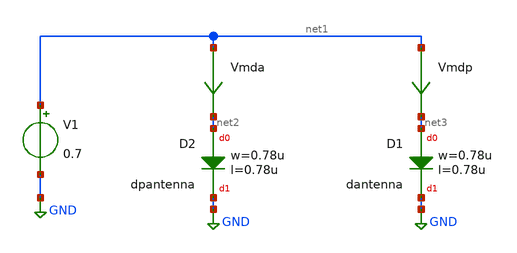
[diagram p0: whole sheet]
** sch_path: ihp-sg13g2/xschem_libs/sg13g2_tests_ase/dc_diode_op/schematic/dc_diode_op.sch
* Copyright 2023 IHP PDK Authors
**.subckt dc_diode_op
V1 net1 GND 0.7
Vmda net1 net2 0
.save i(vmda)
Vmdp net1 net3 0
.save i(vmdp)
XD2 net2 GND dpantenna l=0.78u w=0.78u
XD1 net3 GND dantenna l=0.78u w=0.78u
**.ends
.GLOBAL GND
.end
